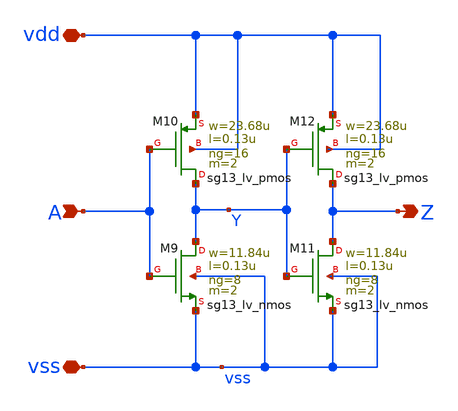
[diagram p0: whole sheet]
** sch_path: v2_feature_extr/d_buff.sch
**.subckt d_buff A Z vdd vss
*.ipin A
*.opin Z
*.iopin vdd
*.iopin vss
XM9 Y A vss vss sg13_lv_nmos w=11.84u l=0.13u ng=8 m=2 mm_ok=1
XM10 Y A vdd vdd sg13_lv_pmos w=23.68u l=0.13u ng=16 m=2 mm_ok=1
XM11 Z Y vss vss sg13_lv_nmos w=11.84u l=0.13u ng=8 m=2 mm_ok=1
XM12 Z Y vdd vdd sg13_lv_pmos w=23.68u l=0.13u ng=16 m=2 mm_ok=1
**.ends
.end
